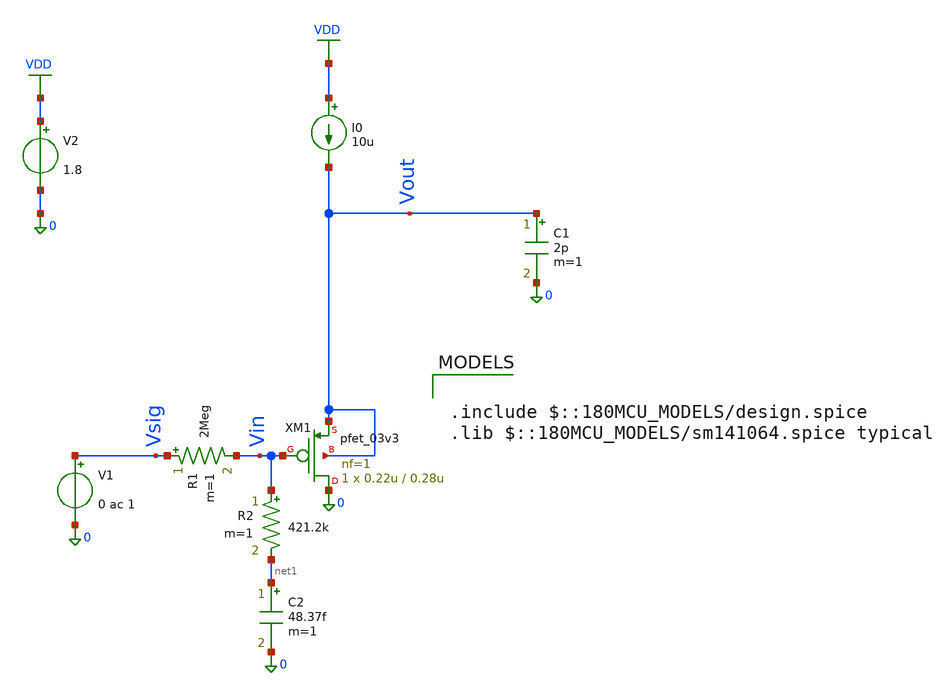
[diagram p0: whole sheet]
** sch_path: Lab_04/Common_Drain.sch
**.subckt Common_Drain
I0 VDD Vout 10u
V1 Vsig 0 0 ac 1
R1 Vsig Vin 2Meg m=1
V2 VDD 0 1.8
C1 Vout 0 2p m=1
R2 Vin net1 421.2k m=1
C2 net1 0 48.37f m=1
XM1 0 Vin Vout Vout pfet_03v3 L=0.28u W=0.22u nf=1 ad=0 as=0 pd=0 ps=0 nrd=0 nrs=0 sa=0 sb=0 sd=0
+ m=1
**** begin user architecture code

.include $::180MCU_MODELS/design.spice
.lib $::180MCU_MODELS/sm141064.spice typical


.control
alterparam sw_stat_global = 0
alterparam sw_stat_mismatch = 0
reset
set outfile = peaking_results.txt
save all
save @m.xm1.m0[id]
save @m.xm1.m0[vgs]
save @m.xm1.m0[vds]
save @m.xm1.m0[vdsat]
save @m.xm1.m0[vth]
save @m.xm1.m0[gm]
save @m.xm1.m0[gds]
save @m.xm1.m0[gmbs]
save @m.xm1.m0[cgs]
save @m.xm1.m0[cgd]
save @m.xm1.m0[csb]
save @m.xm1.m0[cdb]
op
write cd_amp_ac.raw
ac dec 20 1 10g
set appendwrite
write cd_amp_ac.raw
echo "CD Amplifier AC Sim Results" > $outfile
foreach cap 2p 4p 8p
echo "Running Sim using Cap=$cap"
alter c1=$cap
ac dec 20 1 10g
write cd_amp_ac.raw
meas ac gain_peak_cap MAX vdb(vout)
echo "CL = $cap, Gain Peak (dB) = $&gain_peak_cap " >> $outfile
end
* Reset C1 before R sweep
alter c1=2p
foreach my_res 20k 200k 2meg
echo "Running Sim using Res=$my_res"
alter r1=$my_res
ac dec 20 1 10g
write cd_amp_ac.raw
meas ac gain_peak_res MAX vdb(vout)
echo "RES = $my_res, Gain Peak (dB) = $&gain_peak_res " >> $outfile
end
.endc

**** end user architecture code
**.ends
.GLOBAL VDD
.end
